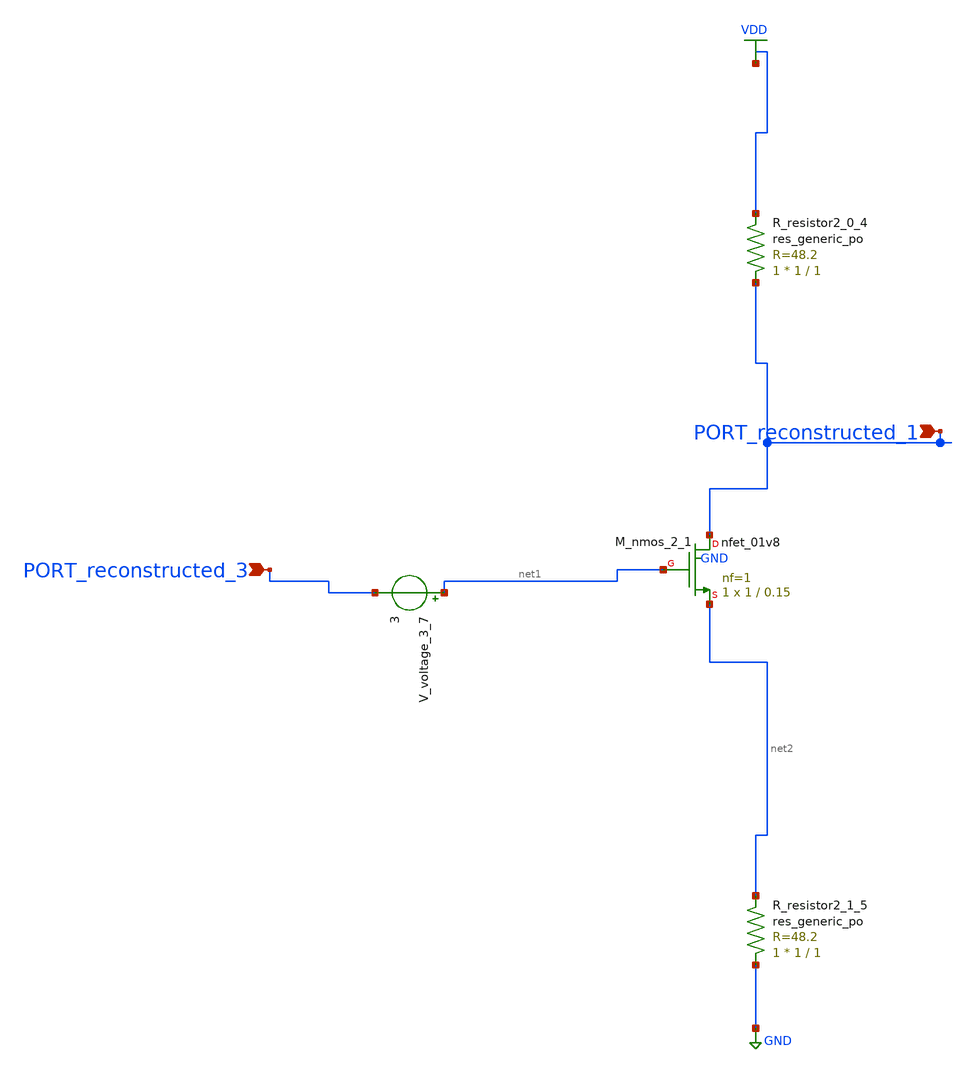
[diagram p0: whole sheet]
** sch_path: schematics/AMSNet/451.sch
**.subckt 451 PORT_reconstructed_1 PORT_reconstructed_3
*.ipin PORT_reconstructed_1
*.ipin PORT_reconstructed_3
XM_nmos_2_1 PORT_reconstructed_1 net1 net2 GND sky130_fd_pr__nfet_01v8 L=0.15 W=1 nf=1 ad='int((1 + 1)/2) * 1 / 1 * 0.29'
+ as='int((1 + 2)/2) * 1 / 1 * 0.29' pd='2*int((1 + 1)/2) * (1 / 1 + 0.29)' ps='2*int((1 + 2)/2) * (1 / 1 + 0.29)'
+ nrd='0.29 / 1 ' nrs='0.29 / 1 ' sa=0 sb=0 sd=0 mult=1 m=1
XR_resistor2_0_4 PORT_reconstructed_1 VDD sky130_fd_pr__res_generic_po W=1 L=1 m=1
XR_resistor2_1_5 GND net2 sky130_fd_pr__res_generic_po W=1 L=1 m=1
V_voltage_3_7 net1 PORT_reconstructed_3 3
**.ends
.GLOBAL GND
.GLOBAL VDD
.end
